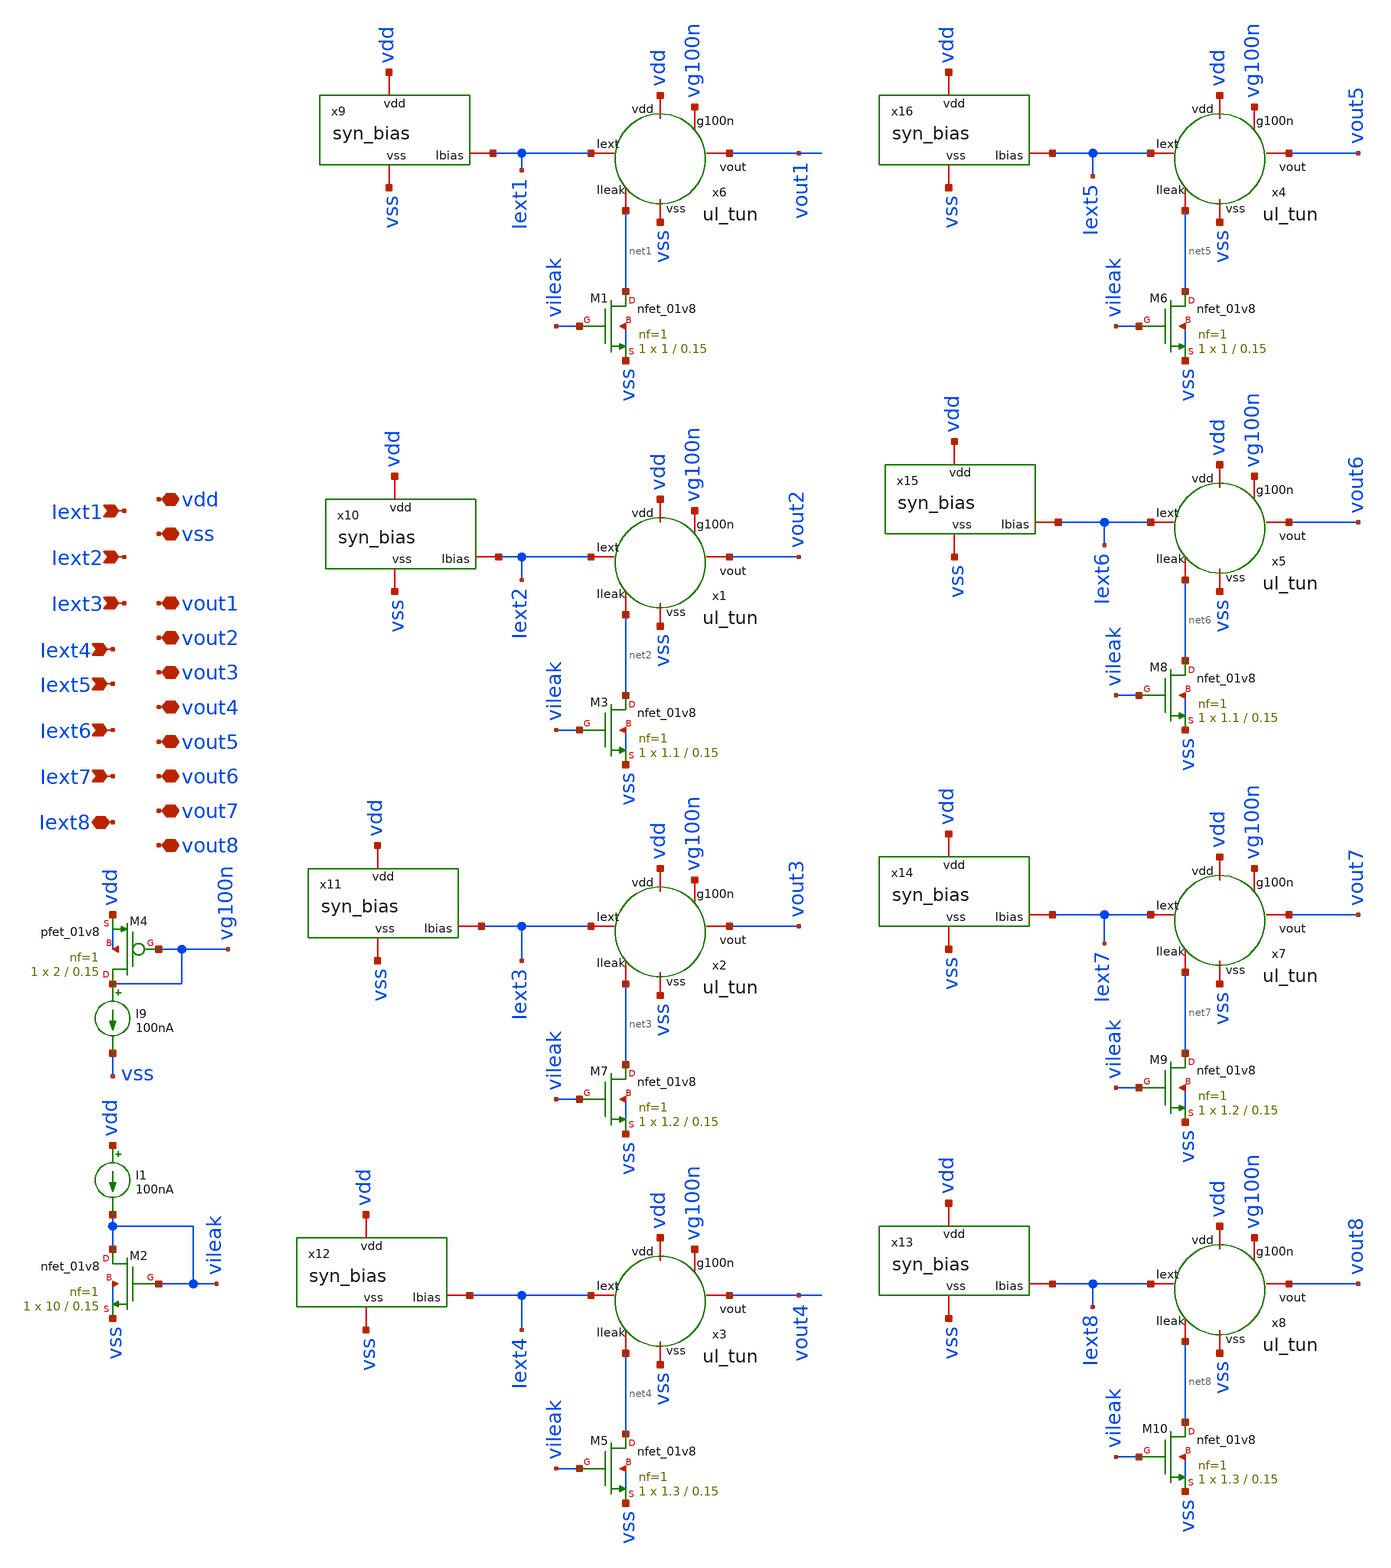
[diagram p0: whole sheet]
** sch_path: layer/layer_hidden.sch
**.subckt layer_hidden vdd vss Iext1 Iext2 Iext3 Iext4 vout1 vout2 vout3 vout4 Iext5 Iext6 Iext7
*+ Iext8 vout5 vout6 vout7 vout8
*.iopin vdd
*.iopin vss
*.ipin Iext1
*.ipin Iext2
*.ipin Iext3
*.ipin Iext4
*.iopin vout1
*.iopin vout2
*.iopin vout3
*.iopin vout4
*.ipin Iext5
*.ipin Iext6
*.ipin Iext7
*.iopin Iext8
*.iopin vout5
*.iopin vout6
*.iopin vout7
*.iopin vout8
x6 Iext1 vdd vg100n vout1 net1 vss ul_tun
I9 vg100n vss 100nA
XM4 vg100n vg100n vdd vdd sky130_fd_pr__pfet_01v8 L=0.15 W=2 nf=1 ad='int((nf+1)/2) * W/nf * 0.29' as='int((nf+2)/2) * W/nf * 0.29'
+ pd='2*int((nf+1)/2) * (W/nf + 0.29)' ps='2*int((nf+2)/2) * (W/nf + 0.29)' nrd='0.29 / W' nrs='0.29 / W'
+ sa=0 sb=0 sd=0 mult=1 m=1
XM1 net1 vileak vss vss sky130_fd_pr__nfet_01v8 L=0.15 W=1 nf=1 ad='int((nf+1)/2) * W/nf * 0.29' as='int((nf+2)/2) * W/nf * 0.29'
+ pd='2*int((nf+1)/2) * (W/nf + 0.29)' ps='2*int((nf+2)/2) * (W/nf + 0.29)' nrd='0.29 / W' nrs='0.29 / W'
+ sa=0 sb=0 sd=0 mult=1 m=1
XM2 vileak vileak vss vss sky130_fd_pr__nfet_01v8 L=0.15 W=10 nf=1 ad='int((nf+1)/2) * W/nf * 0.29' as='int((nf+2)/2) * W/nf * 0.29'
+ pd='2*int((nf+1)/2) * (W/nf + 0.29)' ps='2*int((nf+2)/2) * (W/nf + 0.29)' nrd='0.29 / W' nrs='0.29 / W'
+ sa=0 sb=0 sd=0 mult=1 m=1
I1 vdd vileak 100nA
x1 Iext2 vdd vg100n vout2 net2 vss ul_tun
XM3 net2 vileak vss vss sky130_fd_pr__nfet_01v8 L=0.15 W=1.1 nf=1 ad='int((nf+1)/2) * W/nf * 0.29' as='int((nf+2)/2) * W/nf * 0.29'
+ pd='2*int((nf+1)/2) * (W/nf + 0.29)' ps='2*int((nf+2)/2) * (W/nf + 0.29)' nrd='0.29 / W' nrs='0.29 / W'
+ sa=0 sb=0 sd=0 mult=1 m=1
x2 Iext3 vdd vg100n vout3 net3 vss ul_tun
XM7 net3 vileak vss vss sky130_fd_pr__nfet_01v8 L=0.15 W=1.2 nf=1 ad='int((nf+1)/2) * W/nf * 0.29' as='int((nf+2)/2) * W/nf * 0.29'
+ pd='2*int((nf+1)/2) * (W/nf + 0.29)' ps='2*int((nf+2)/2) * (W/nf + 0.29)' nrd='0.29 / W' nrs='0.29 / W'
+ sa=0 sb=0 sd=0 mult=1 m=1
x3 Iext4 vdd vg100n vout4 net4 vss ul_tun
XM5 net4 vileak vss vss sky130_fd_pr__nfet_01v8 L=0.15 W=1.3 nf=1 ad='int((nf+1)/2) * W/nf * 0.29' as='int((nf+2)/2) * W/nf * 0.29'
+ pd='2*int((nf+1)/2) * (W/nf + 0.29)' ps='2*int((nf+2)/2) * (W/nf + 0.29)' nrd='0.29 / W' nrs='0.29 / W'
+ sa=0 sb=0 sd=0 mult=1 m=1
x4 Iext5 vdd vg100n vout5 net5 vss ul_tun
XM6 net5 vileak vss vss sky130_fd_pr__nfet_01v8 L=0.15 W=1 nf=1 ad='int((nf+1)/2) * W/nf * 0.29' as='int((nf+2)/2) * W/nf * 0.29'
+ pd='2*int((nf+1)/2) * (W/nf + 0.29)' ps='2*int((nf+2)/2) * (W/nf + 0.29)' nrd='0.29 / W' nrs='0.29 / W'
+ sa=0 sb=0 sd=0 mult=1 m=1
x5 Iext6 vdd vg100n vout6 net6 vss ul_tun
XM8 net6 vileak vss vss sky130_fd_pr__nfet_01v8 L=0.15 W=1.1 nf=1 ad='int((nf+1)/2) * W/nf * 0.29' as='int((nf+2)/2) * W/nf * 0.29'
+ pd='2*int((nf+1)/2) * (W/nf + 0.29)' ps='2*int((nf+2)/2) * (W/nf + 0.29)' nrd='0.29 / W' nrs='0.29 / W'
+ sa=0 sb=0 sd=0 mult=1 m=1
x7 Iext7 vdd vg100n vout7 net7 vss ul_tun
XM9 net7 vileak vss vss sky130_fd_pr__nfet_01v8 L=0.15 W=1.2 nf=1 ad='int((nf+1)/2) * W/nf * 0.29' as='int((nf+2)/2) * W/nf * 0.29'
+ pd='2*int((nf+1)/2) * (W/nf + 0.29)' ps='2*int((nf+2)/2) * (W/nf + 0.29)' nrd='0.29 / W' nrs='0.29 / W'
+ sa=0 sb=0 sd=0 mult=1 m=1
x8 Iext8 vdd vg100n vout8 net8 vss ul_tun
XM10 net8 vileak vss vss sky130_fd_pr__nfet_01v8 L=0.15 W=1.3 nf=1 ad='int((nf+1)/2) * W/nf * 0.29' as='int((nf+2)/2) * W/nf * 0.29'
+ pd='2*int((nf+1)/2) * (W/nf + 0.29)' ps='2*int((nf+2)/2) * (W/nf + 0.29)' nrd='0.29 / W' nrs='0.29 / W'
+ sa=0 sb=0 sd=0 mult=1 m=1
x9 vdd vss Iext1 syn_bias
x10 vdd vss Iext2 syn_bias
x11 vdd vss Iext3 syn_bias
x12 vdd vss Iext4 syn_bias
x13 vdd vss Iext8 syn_bias
x14 vdd vss Iext7 syn_bias
x15 vdd vss Iext6 syn_bias
x16 vdd vss Iext5 syn_bias
**.ends

* expanding   symbol:  Neuron/ultralif/ul_tun.sym # of pins=6
** sym_path: Neuron/ultralif/ul_tun.sym
** sch_path: Neuron/ultralif/ul_tun.sch
.subckt ul_tun Iext vdd g100n vout Ileak vss
*.iopin Iext
*.iopin vout
*.iopin vss
*.iopin Ileak
*.iopin vdd
*.iopin g100n
XM1 Ileak Ileak net1 vdd sky130_fd_pr__pfet_01v8 L=10 W=1 nf=1 ad='int((nf+1)/2) * W/nf * 0.29' as='int((nf+2)/2) * W/nf * 0.29'
+ pd='2*int((nf+1)/2) * (W/nf + 0.29)' ps='2*int((nf+2)/2) * (W/nf + 0.29)' nrd='0.29 / W' nrs='0.29 / W'
+ sa=0 sb=0 sd=0 mult=1 m=1
XM2 Ileak net2 net1 vdd sky130_fd_pr__pfet_01v8 L=0.15 W=1.5 nf=1 ad='int((nf+1)/2) * W/nf * 0.29' as='int((nf+2)/2) * W/nf * 0.29'
+ pd='2*int((nf+1)/2) * (W/nf + 0.29)' ps='2*int((nf+2)/2) * (W/nf + 0.29)' nrd='0.29 / W' nrs='0.29 / W'
+ sa=0 sb=0 sd=0 mult=1 m=1
XM3 net2 net2 net1 vdd sky130_fd_pr__pfet_01v8 L=0.15 W=15 nf=1 ad='int((nf+1)/2) * W/nf * 0.29' as='int((nf+2)/2) * W/nf * 0.29'
+ pd='2*int((nf+1)/2) * (W/nf + 0.29)' ps='2*int((nf+2)/2) * (W/nf + 0.29)' nrd='0.29 / W' nrs='0.29 / W'
+ sa=0 sb=0 sd=0 mult=1 m=1
XM4 net2 Ileak vss vss sky130_fd_pr__nfet_01v8 L=4 W=1 nf=1 ad='int((1 + 1)/2) * 1 / 1 * 0.29' as='int((1 + 2)/2) * 1 / 1 * 0.29'
+ pd='2*int((1 + 1)/2) * (1 / 1 + 0.29)' ps='2*int((1 + 2)/2) * (1 / 1 + 0.29)' nrd='0.29 / 1 ' nrs='0.29 / 1 '
+ sa=0 sb=0 sd=0 mult=1 m=1
C1 net1 vss 1p m=1
XM5 vout_n Ileak vss vss sky130_fd_pr__nfet_01v8 L=0.15 W=1 nf=1 ad='int((1 + 1)/2) * 1 / 1 * 0.29' as='int((1 + 2)/2) * 1 / 1 * 0.29'
+ pd='2*int((1 + 1)/2) * (1 / 1 + 0.29)' ps='2*int((1 + 2)/2) * (1 / 1 + 0.29)' nrd='0.29 / 1 ' nrs='0.29 / 1 '
+ sa=0 sb=0 sd=0 mult=1 m=1
XM6 vout_n g100n vdd vdd sky130_fd_pr__pfet_01v8 L=0.15 W=2 nf=1 ad='int((nf+1)/2) * W/nf * 0.29' as='int((nf+2)/2) * W/nf * 0.29'
+ pd='2*int((nf+1)/2) * (W/nf + 0.29)' ps='2*int((nf+2)/2) * (W/nf + 0.29)' nrd='0.29 / W' nrs='0.29 / W'
+ sa=0 sb=0 sd=0 mult=1 m=1
XM7 vout vout_n vss vss sky130_fd_pr__nfet_01v8 L=0.15 W=1 nf=1 ad='int((1 + 1)/2) * 1 / 1 * 0.29' as='int((1 + 2)/2) * 1 / 1 * 0.29'
+ pd='2*int((1 + 1)/2) * (1 / 1 + 0.29)' ps='2*int((1 + 2)/2) * (1 / 1 + 0.29)' nrd='0.29 / 1 ' nrs='0.29 / 1 '
+ sa=0 sb=0 sd=0 mult=1 m=1
XM8 vout vout_n vdd vdd sky130_fd_pr__pfet_01v8 L=0.15 W=2 nf=1 ad='int((nf+1)/2) * W/nf * 0.29' as='int((nf+2)/2) * W/nf * 0.29'
+ pd='2*int((nf+1)/2) * (W/nf + 0.29)' ps='2*int((nf+2)/2) * (W/nf + 0.29)' nrd='0.29 / W' nrs='0.29 / W'
+ sa=0 sb=0 sd=0 mult=1 m=1
XM9 net3 Ileak Iext vdd sky130_fd_pr__pfet_01v8 L=0.15 W=4 nf=1 ad='int((nf+1)/2) * W/nf * 0.29' as='int((nf+2)/2) * W/nf * 0.29'
+ pd='2*int((nf+1)/2) * (W/nf + 0.29)' ps='2*int((nf+2)/2) * (W/nf + 0.29)' nrd='0.29 / W' nrs='0.29 / W'
+ sa=0 sb=0 sd=0 mult=1 m=1
vext net3 net1 0
**** begin user architecture code


.save i(vext) v(vout)


**** end user architecture code
.ends


* expanding   symbol:  /home/alex/Desktop/EDA/SNN_IPN/Neuron/ultralif/syn_bias.sym # of pins=3
** sym_path: Neuron/ultralif/syn_bias.sym
** sch_path: Neuron/ultralif/syn_bias.sch
.subckt syn_bias vdd vss Ibias
*.iopin vss
*.iopin vdd
*.iopin Ibias
XM2 Ibias net1 vdd vdd sky130_fd_pr__pfet_01v8 L=1 W=0.5 nf=1 ad='int((nf+1)/2) * W/nf * 0.29' as='int((nf+2)/2) * W/nf * 0.29'
+ pd='2*int((nf+1)/2) * (W/nf + 0.29)' ps='2*int((nf+2)/2) * (W/nf + 0.29)' nrd='0.29 / W' nrs='0.29 / W'
+ sa=0 sb=0 sd=0 mult=1 m=1
XR1 net1 vdd sky130_fd_pr__res_generic_po W=1.15 L=1 m=1
XR2 vss net1 sky130_fd_pr__res_generic_po W=1 L=1 m=1
.ends

.end
